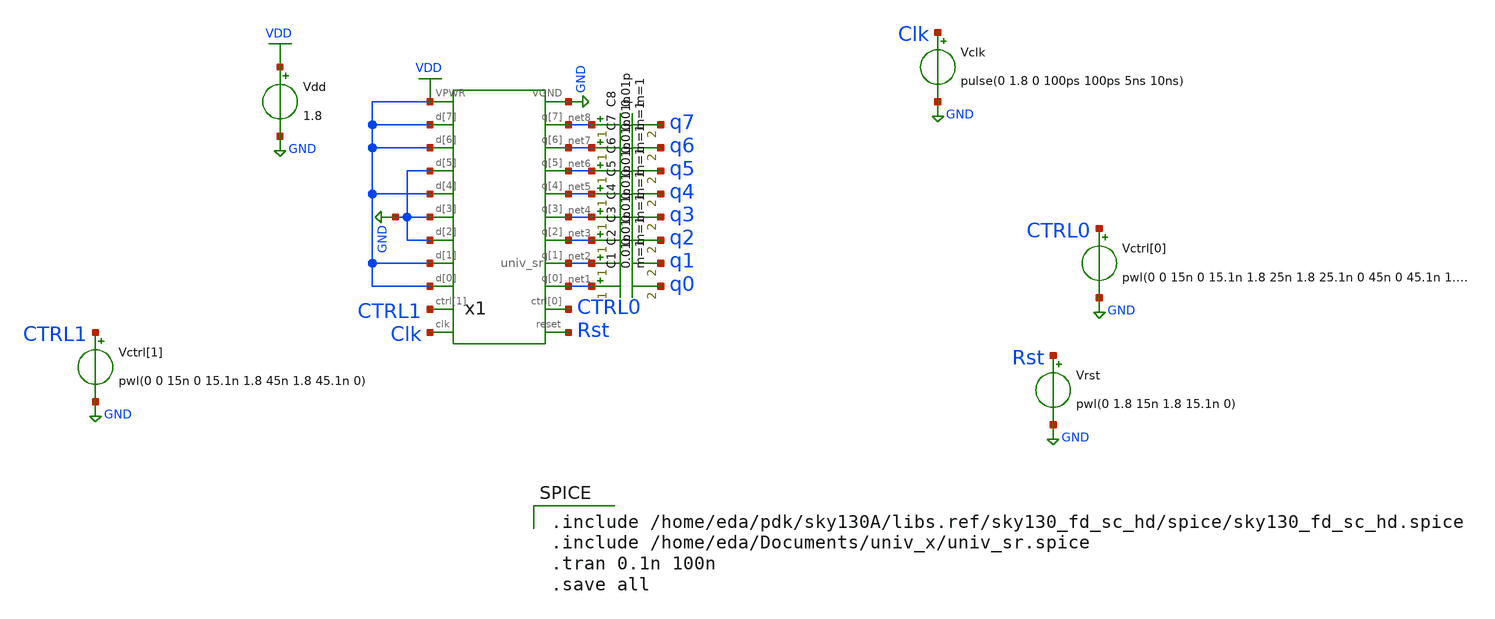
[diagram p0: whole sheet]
** sch_path: schematics/final_tb.sch
**.subckt final_tb
Vdd VDD GND 1.8
Vclk Clk GND pulse(0 1.8 0 100ps 100ps 5ns 10ns)
Vrst Rst GND pwl(0 1.8 15n 1.8 15.1n 0)
Vctrl[1] CTRL1 GND pwl(0 0 15n 0 15.1n 1.8 45n 1.8 45.1n 0)
Vctrl[0] CTRL0 GND pwl(0 0 15n 0 15.1n 1.8 25n 1.8 25.1n 0 45n 0 45.1n 1.8 65n 1.8 65.1n 0)
x1 GND VDD Clk CTRL0 CTRL1 VDD VDD GND GND VDD GND VDD VDD net1 net2 net3 net4 net5 net6 net7 net8
+ Rst univ_sr
C1 net1 q0 0.01p m=1
C2 net2 q1 0.01p m=1
C3 net3 q2 0.01p m=1
C4 net4 q3 0.01p m=1
C5 net5 q4 0.01p m=1
C6 net6 q5 0.01p m=1
C7 net7 q6 0.01p m=1
C8 net8 q7 0.01p m=1
**** begin user architecture code

.include /home/eda/pdk/sky130A/libs.ref/sky130_fd_sc_hd/spice/sky130_fd_sc_hd.spice
.include /home/eda/Documents/univ_x/univ_sr.spice
.tran 0.1n 100n
.save all


** opencircuitdesign pdks install
.lib $::SKYWATER_MODELS/sky130.lib.spice tt


**** end user architecture code
**.ends
.GLOBAL VDD
.GLOBAL GND
.end
